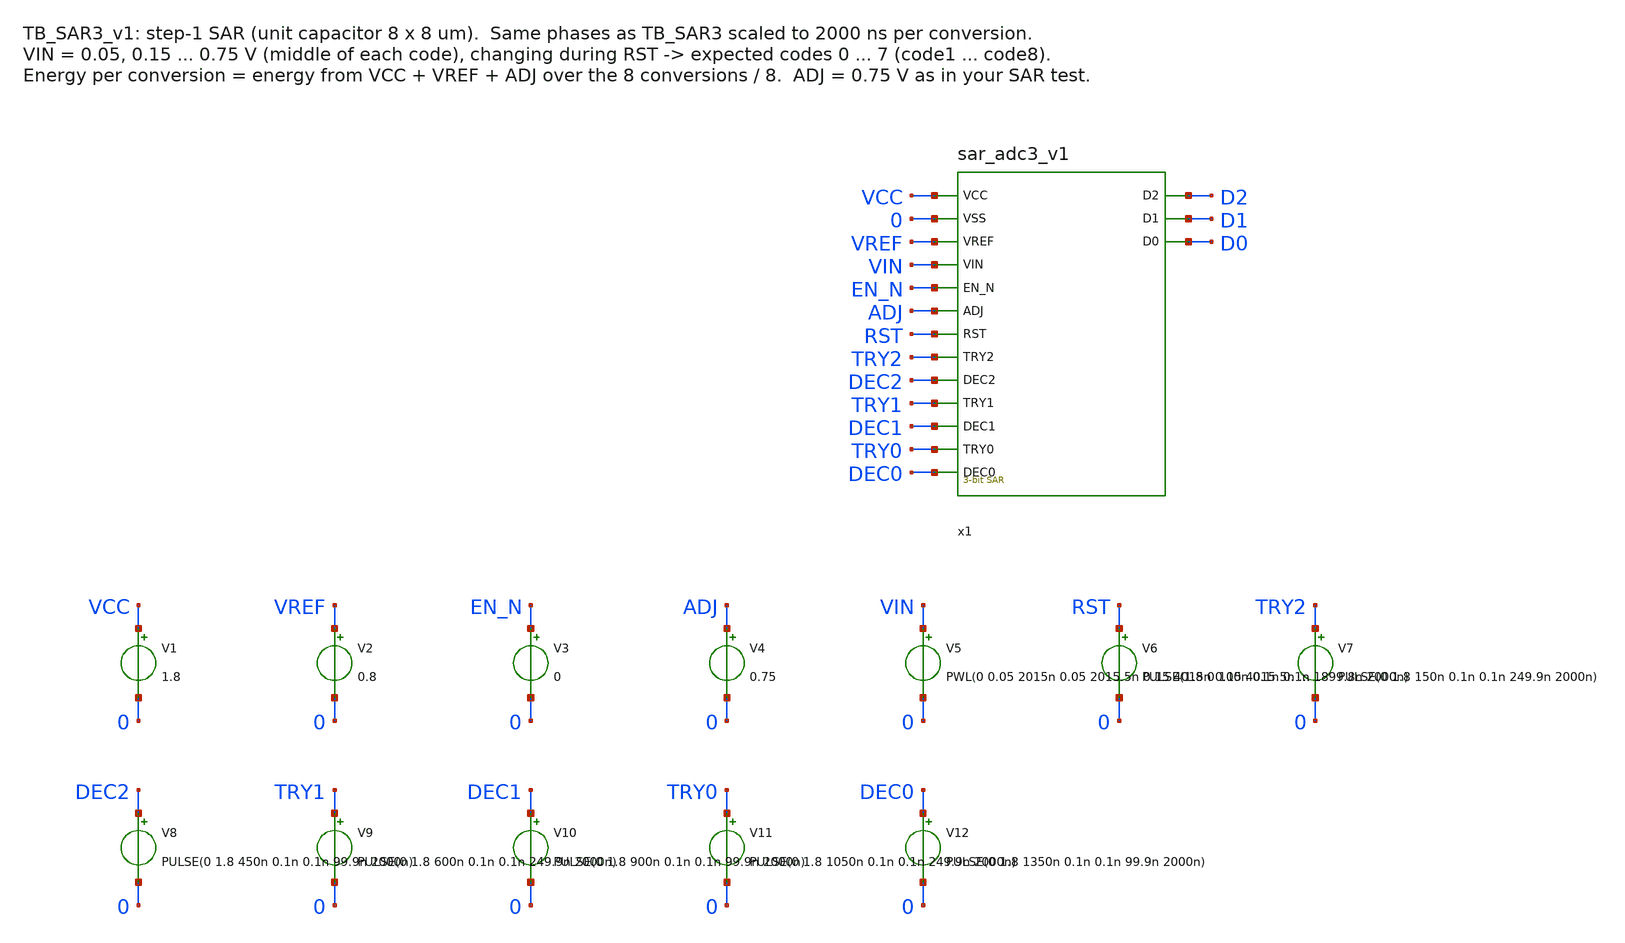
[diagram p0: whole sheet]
** sch_path: SAR_improved/TB_SAR3_v1.sch
**.subckt TB_SAR3_v1
x1 VCC 0 VREF VIN EN_N ADJ RST TRY2 DEC2 TRY1 DEC1 TRY0 DEC0 D2 D1 D0 sar_adc3_v1
V1 VCC 0 1.8
V2 VREF 0 0.8
V3 EN_N 0 0
V4 ADJ 0 0.75
V5 VIN 0 PWL(0 0.05 2015n 0.05 2015.5n 0.15 4015n 0.15 4015.5n 0.25 6015n 0.25 6015.5n 0.35 8015n
+ 0.35 8015.5n 0.45 10015n 0.45 10015.5n 0.55 12015n 0.55 12015.5n 0.65 14015n 0.65 14015.5n 0.75)
V6 RST 0 PULSE(1.8 0 100n 0.1n 0.1n 1899.8n 2000n)
V7 TRY2 0 PULSE(0 1.8 150n 0.1n 0.1n 249.9n 2000n)
V8 DEC2 0 PULSE(0 1.8 450n 0.1n 0.1n 99.9n 2000n)
V9 TRY1 0 PULSE(0 1.8 600n 0.1n 0.1n 249.9n 2000n)
V10 DEC1 0 PULSE(0 1.8 900n 0.1n 0.1n 99.9n 2000n)
V11 TRY0 0 PULSE(0 1.8 1050n 0.1n 0.1n 249.9n 2000n)
V12 DEC0 0 PULSE(0 1.8 1350n 0.1n 0.1n 99.9n 2000n)
**** begin user architecture code

.lib /home/ttuser/pdk/sky130A/libs.tech/combined/sky130.lib.spice tt
.option method=gear reltol=1e-4
.control
save all
tran 0.5n 16000n
let code = 4*ceil((v(D2)-0.9)/10) + 2*ceil((v(D1)-0.9)/10) + ceil((v(D0)-0.9)/10)
meas tran code1 find code at=1600n
meas tran code2 find code at=3600n
meas tran code3 find code at=5600n
meas tran code4 find code at=7600n
meas tran code5 find code at=9600n
meas tran code6 find code at=11600n
meas tran code7 find code at=13600n
meas tran code8 find code at=15600n
let ptot = 1.8*(-i(V1)) + 0.8*(-i(V2)) + 0.75*(-i(V4))
meas tran etot integ ptot from=0 to=16000n
let e_conv_pJ = etot/8*1e12
let p_uW = etot/16000e-9*1e6
print e_conv_pJ p_uW
plot v(VIN) v(x1.REF)
plot v(D2) v(D1)+2 v(D0)+4
plot code v(VIN)
.endc

**** end user architecture code
**.ends
.end
